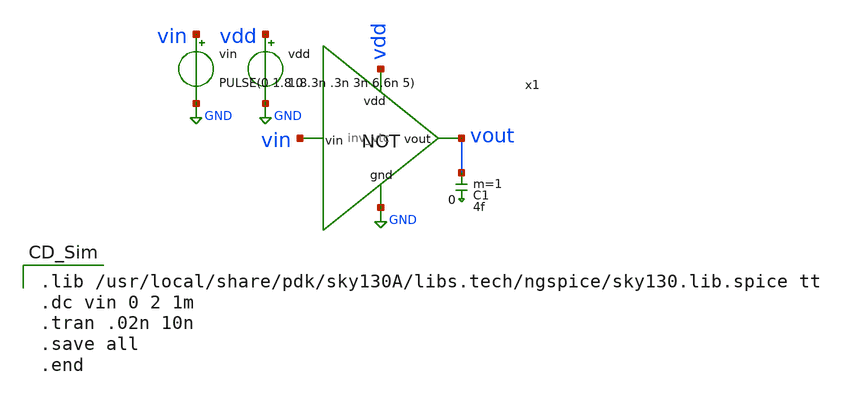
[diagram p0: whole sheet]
** sch_path: working_dir/inverter_tb.sch
**.subckt inverter_tb
x1 vdd vin vout GND inv_vtc
vin vin GND PULSE(0 1.8 0 .3n .3n 3n 6.6n 5)
vdd vdd GND 1.8
C1 vout 0 4f m=1
**** begin user architecture code

.lib /usr/local/share/pdk/sky130A/libs.tech/ngspice/sky130.lib.spice tt
.dc vin 0 2 1m
.tran .02n 10n
.save all
.end

**** end user architecture code
**.ends
.GLOBAL GND
.end
